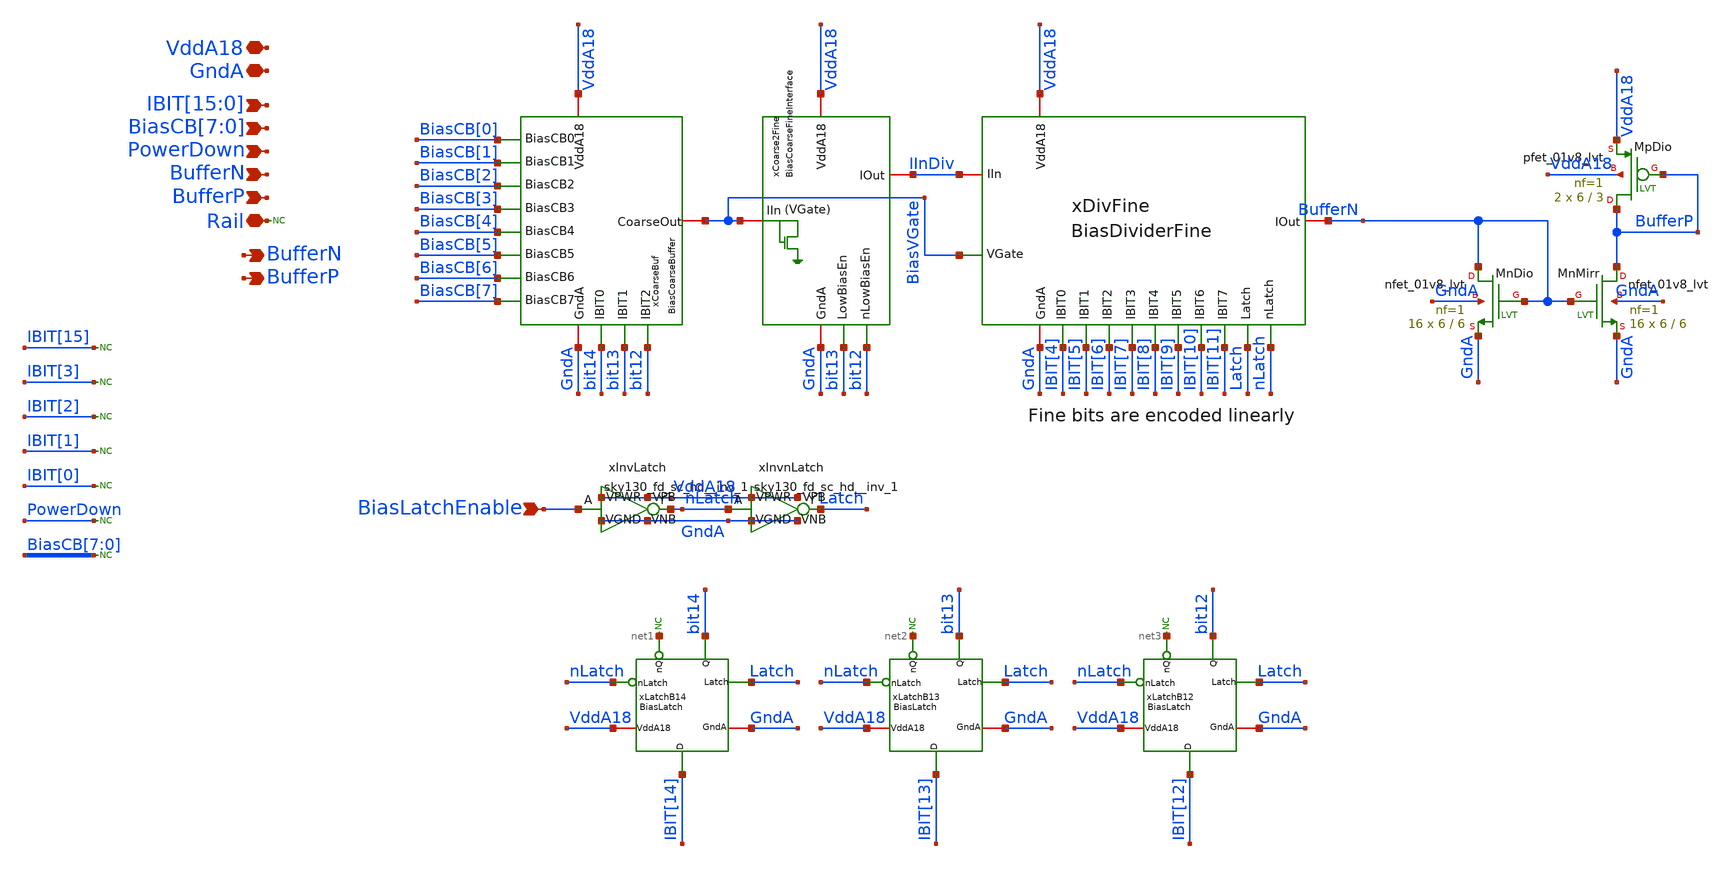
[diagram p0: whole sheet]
** sch_path: analog/xschem/BiasBranchBuffer.sch
**.subckt BiasBranchBuffer VddA18 GndA BufferN BiasLatchEnable
*+ IBIT[15],IBIT[14],IBIT[13],IBIT[12],IBIT[11],IBIT[10],IBIT[9],IBIT[8],IBIT[7],IBIT[6],IBIT[5],IBIT[4],IBIT[3],IBIT[2],IBIT[1],IBIT[0] BiasCB[7],BiasCB[6],BiasCB[5],BiasCB[4],BiasCB[3],BiasCB[2],BiasCB[1],BiasCB[0] PowerDown BufferN
*+ BufferP Rail BufferP
*.iopin VddA18
*.iopin GndA
*.opin BufferN
*.ipin BiasLatchEnable
*.ipin
*+ IBIT[15],IBIT[14],IBIT[13],IBIT[12],IBIT[11],IBIT[10],IBIT[9],IBIT[8],IBIT[7],IBIT[6],IBIT[5],IBIT[4],IBIT[3],IBIT[2],IBIT[1],IBIT[0]
*.ipin BiasCB[7],BiasCB[6],BiasCB[5],BiasCB[4],BiasCB[3],BiasCB[2],BiasCB[1],BiasCB[0]
*.ipin PowerDown
*.ipin BufferN
*.ipin BufferP
*.iopin Rail
*.opin BufferP
xCoarseBuf VddA18 GndA bit14 bit13 bit12 BiasVGate BiasCB[0] BiasCB[1] BiasCB[3] BiasCB[4] BiasCB[5]
+ BiasCB[6] BiasCB[7] BiasCB[2] BiasCoarseBuffer
xCoarse2Fine VddA18 GndA bit13 bit12 BiasVGate IInDiv BiasCoarseFineInterface
xDivFine VddA18 GndA IBIT[4] IBIT[5] IInDiv BufferN IBIT[6] IBIT[7] IBIT[8] IBIT[9] IBIT[10]
+ IBIT[11] Latch nLatch BiasVGate BiasDividerFine
xLatchB14 VddA18 GndA net1 bit14 Latch nLatch IBIT[14] BiasLatch
* noconn #net1
xLatchB13 VddA18 GndA net2 bit13 Latch nLatch IBIT[13] BiasLatch
* noconn #net2
xLatchB12 VddA18 GndA net3 bit12 Latch nLatch IBIT[12] BiasLatch
* noconn #net3
* noconn IBIT[15]
* noconn IBIT[3]
* noconn IBIT[2]
* noconn IBIT[1]
* noconn IBIT[0]
XMpDio BufferP BufferP VddA18 VddA18 sky130_fd_pr__pfet_01v8_lvt L=3 W=6 nf=1 ad='int((1 + 1)/2) * 6 / 1 * 0.29'
+ as='int((1 + 2)/2) * 6 / 1 * 0.29' pd='2*int((1 + 1)/2) * (6 / 1 + 0.29)' ps='2*int((1 + 2)/2) * (6 / 1 + 0.29)'
+ nrd='0.29 / 6 ' nrs='0.29 / 6 ' sa=0 sb=0 sd=0 mult=2 m=2
XMnDio BufferN BufferN GndA GndA sky130_fd_pr__nfet_01v8_lvt L=6 W=6 nf=1 ad='int((1 + 1)/2) * 6 / 1 * 0.29'
+ as='int((1 + 2)/2) * 6 / 1 * 0.29' pd='2*int((1 + 1)/2) * (6 / 1 + 0.29)' ps='2*int((1 + 2)/2) * (6 / 1 + 0.29)'
+ nrd='0.29 / 6 ' nrs='0.29 / 6 ' sa=0 sb=0 sd=0 mult=16 m=16
XMnMirr BufferP BufferN GndA GndA sky130_fd_pr__nfet_01v8_lvt L=6 W=6 nf=1 ad='int((1 + 1)/2) * 6 / 1 * 0.29'
+ as='int((1 + 2)/2) * 6 / 1 * 0.29' pd='2*int((1 + 1)/2) * (6 / 1 + 0.29)' ps='2*int((1 + 2)/2) * (6 / 1 + 0.29)'
+ nrd='0.29 / 6 ' nrs='0.29 / 6 ' sa=0 sb=0 sd=0 mult=16 m=16
* noconn PowerDown
* noconn BiasCB[7:0]
* noconn Rail
xInvLatch BiasLatchEnable nLatch VddA18 VddA18 GndA GndA sky130_fd_sc_hd__inv_1
xInvnLatch nLatch Latch VddA18 VddA18 GndA GndA sky130_fd_sc_hd__inv_1
**.ends
.end
